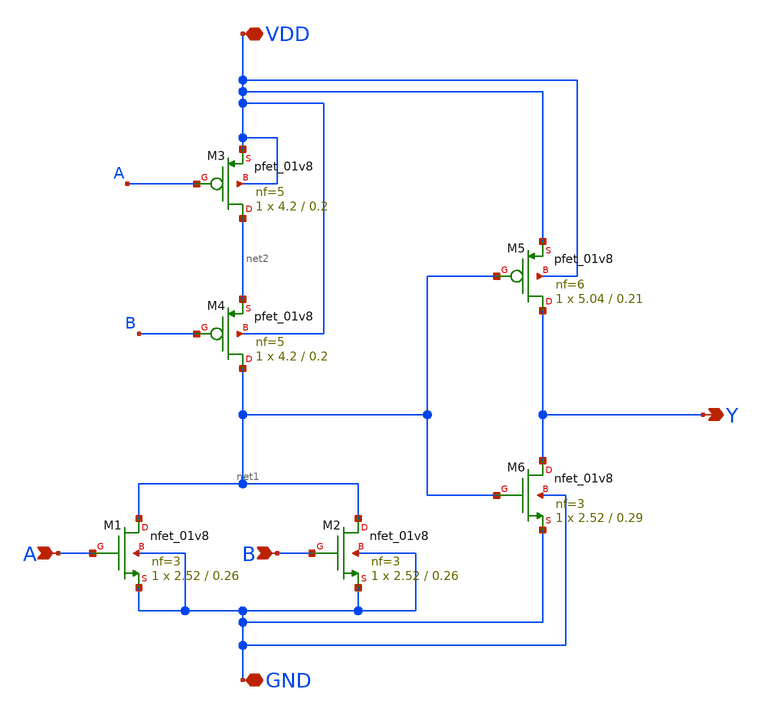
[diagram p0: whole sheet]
** sch_path: cells/OR2X4/schematic/or2x4.sch
**.subckt or2x4 A B VDD GND Y
*.ipin A
*.ipin B
*.iopin VDD
*.iopin GND
*.opin Y
XM1 net1 A GND GND sky130_fd_pr__nfet_01v8 L=0.26 W=2.52 nf=3 ad='int((3 + 1)/2) * 2.52 / 3 * 0.29' as='int((3 + 2)/2) * 2.52 / 3 * 0.29'
+ pd='2*int((3 + 1)/2) * (2.52 / 3 + 0.29)' ps='2*int((3 + 2)/2) * (2.52 / 3 + 0.29)' nrd='0.29 / 2.52 '
+ nrs='0.29 / 2.52 ' sa=0 sb=0 sd=0 mult=1 m=1
XM3 net2 A VDD VDD sky130_fd_pr__pfet_01v8 L=0.2 W=4.2 nf=5 ad='int((5 + 1)/2) * 4.2 / 5 * 0.29' as='int((5 + 2)/2) * 4.2 / 5 * 0.29'
+ pd='2*int((5 + 1)/2) * (4.2 / 5 + 0.29)' ps='2*int((5 + 2)/2) * (4.2 / 5 + 0.29)' nrd='0.29 / 4.2 ' nrs='0.29 / 4.2 '
+ sa=0 sb=0 sd=0 mult=1 m=1
XM5 Y net1 VDD VDD sky130_fd_pr__pfet_01v8 L=0.21 W=5.04 nf=6 ad='int((6 + 1)/2) * 5.04 / 6 * 0.29' as='int((6 + 2)/2) * 5.04 / 6 * 0.29'
+ pd='2*int((6 + 1)/2) * (5.04 / 6 + 0.29)' ps='2*int((6 + 2)/2) * (5.04 / 6 + 0.29)' nrd='0.29 / 5.04 '
+ nrs='0.29 / 5.04 ' sa=0 sb=0 sd=0 mult=1 m=1
XM4 net1 B net2 VDD sky130_fd_pr__pfet_01v8 L=0.2 W=4.2 nf=5 ad='int((5 + 1)/2) * 4.2 / 5 * 0.29' as='int((5 + 2)/2) * 4.2 / 5 * 0.29'
+ pd='2*int((5 + 1)/2) * (4.2 / 5 + 0.29)' ps='2*int((5 + 2)/2) * (4.2 / 5 + 0.29)' nrd='0.29 / 4.2 ' nrs='0.29 / 4.2 '
+ sa=0 sb=0 sd=0 mult=1 m=1
XM2 net1 B GND GND sky130_fd_pr__nfet_01v8 L=0.26 W=2.52 nf=3 ad='int((3 + 1)/2) * 2.52 / 3 * 0.29' as='int((3 + 2)/2) * 2.52 / 3 * 0.29'
+ pd='2*int((3 + 1)/2) * (2.52 / 3 + 0.29)' ps='2*int((3 + 2)/2) * (2.52 / 3 + 0.29)' nrd='0.29 / 2.52 '
+ nrs='0.29 / 2.52 ' sa=0 sb=0 sd=0 mult=1 m=1
XM6 Y net1 GND GND sky130_fd_pr__nfet_01v8 L=0.29 W=2.52 nf=3 ad='int((3 + 1)/2) * 2.52 / 3 * 0.29' as='int((3 + 2)/2) * 2.52 / 3 * 0.29'
+ pd='2*int((3 + 1)/2) * (2.52 / 3 + 0.29)' ps='2*int((3 + 2)/2) * (2.52 / 3 + 0.29)' nrd='0.29 / 2.52 '
+ nrs='0.29 / 2.52 ' sa=0 sb=0 sd=0 mult=1 m=1
**.ends
.end
